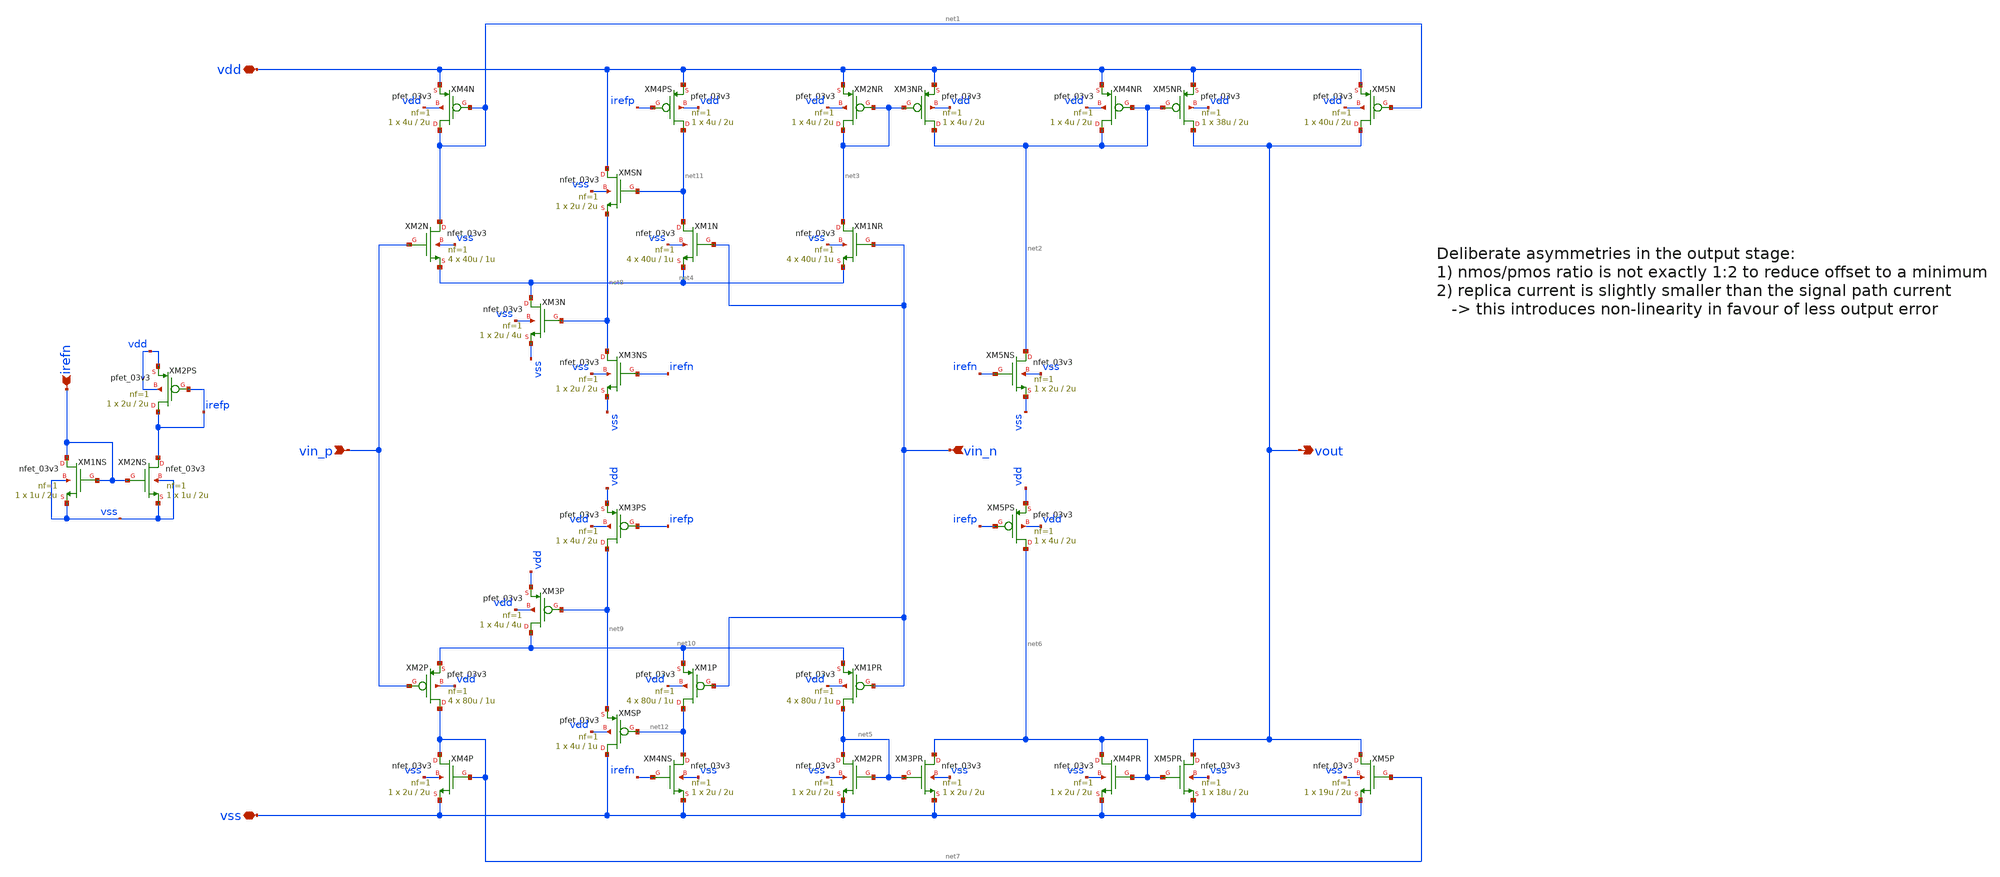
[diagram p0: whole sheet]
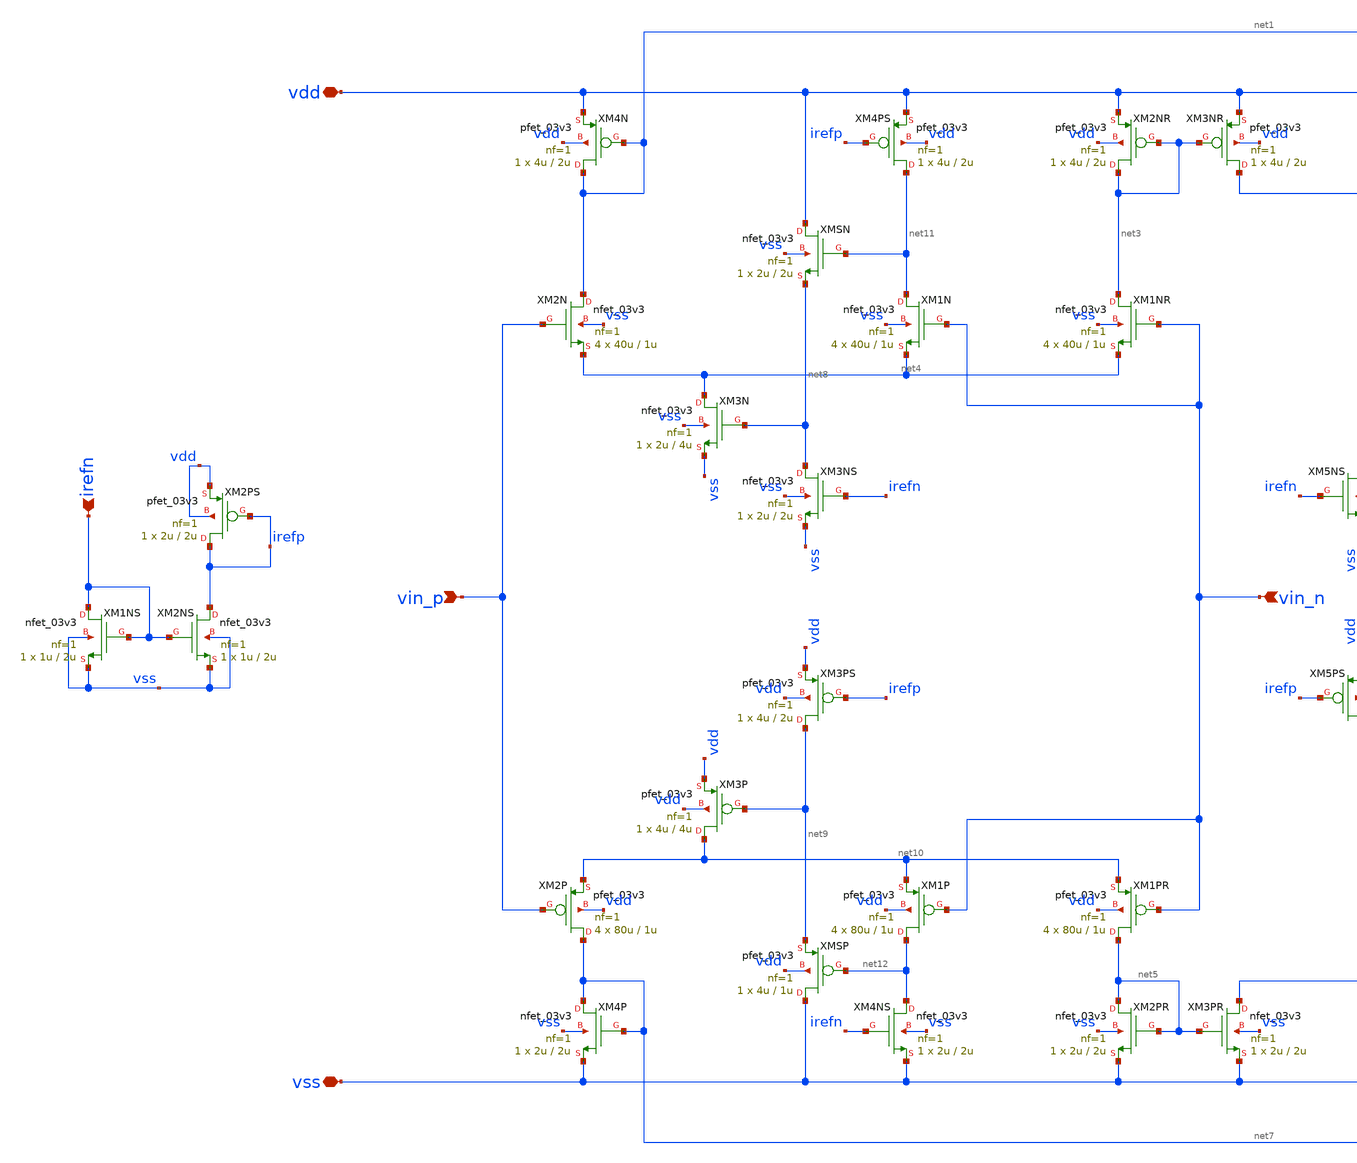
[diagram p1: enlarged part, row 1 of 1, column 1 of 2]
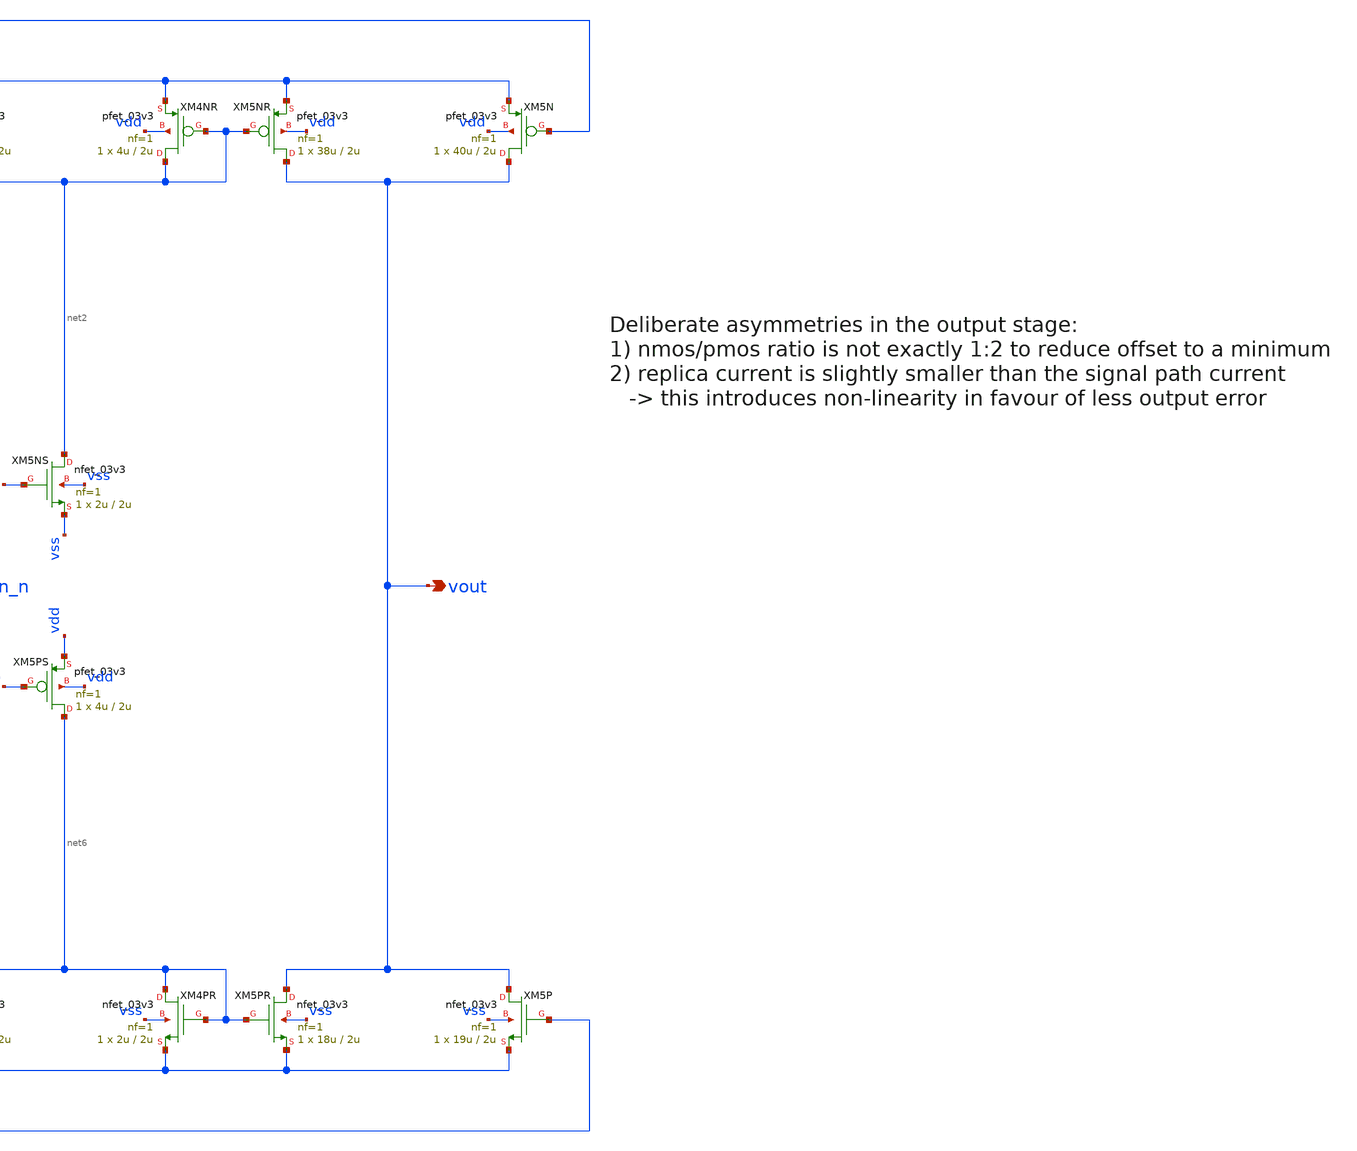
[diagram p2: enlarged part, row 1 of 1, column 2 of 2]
** sch_path: General/ADC/analogbuffer/analogbuffer-openloop.sch
**.subckt analogbuffer-openloop vdd vss vin_p vout irefn vin_n
*.iopin vdd
*.iopin vss
*.ipin vin_p
*.opin vout
*.ipin irefn
*.ipin vin_n
XM2P net7 vin_p net10 vdd pfet_03v3 L=1u W=80u nf=1 ad='int((nf+1)/2) * W/nf * 0.18u' as='int((nf+2)/2) * W/nf * 0.18u'
+ pd='2*int((nf+1)/2) * (W/nf + 0.18u)' ps='2*int((nf+2)/2) * (W/nf + 0.18u)' nrd='0.18u / W' nrs='0.18u / W'
+ sa=0 sb=0 sd=0 m=4
XM2N net1 vin_p net4 vss nfet_03v3 L=1u W=40u nf=1 ad='int((nf+1)/2) * W/nf * 0.18u' as='int((nf+2)/2) * W/nf * 0.18u'
+ pd='2*int((nf+1)/2) * (W/nf + 0.18u)' ps='2*int((nf+2)/2) * (W/nf + 0.18u)' nrd='0.18u / W' nrs='0.18u / W'
+ sa=0 sb=0 sd=0 m=4
XM3N net4 net8 vss vss nfet_03v3 L=4u W=2u nf=1 ad='int((nf+1)/2) * W/nf * 0.18u' as='int((nf+2)/2) * W/nf * 0.18u'
+ pd='2*int((nf+1)/2) * (W/nf + 0.18u)' ps='2*int((nf+2)/2) * (W/nf + 0.18u)' nrd='0.18u / W' nrs='0.18u / W'
+ sa=0 sb=0 sd=0 m=1
XM1NR net3 vin_n net4 vss nfet_03v3 L=1u W=40u nf=1 ad='int((nf+1)/2) * W/nf * 0.18u' as='int((nf+2)/2) * W/nf * 0.18u'
+ pd='2*int((nf+1)/2) * (W/nf + 0.18u)' ps='2*int((nf+2)/2) * (W/nf + 0.18u)' nrd='0.18u / W' nrs='0.18u / W'
+ sa=0 sb=0 sd=0 m=4
XM2NR net3 net3 vdd vdd pfet_03v3 L=2u W=4u nf=1 ad='int((nf+1)/2) * W/nf * 0.18u' as='int((nf+2)/2) * W/nf * 0.18u'
+ pd='2*int((nf+1)/2) * (W/nf + 0.18u)' ps='2*int((nf+2)/2) * (W/nf + 0.18u)' nrd='0.18u / W' nrs='0.18u / W'
+ sa=0 sb=0 sd=0 m=1
XM3NR net2 net3 vdd vdd pfet_03v3 L=2u W=4u nf=1 ad='int((nf+1)/2) * W/nf * 0.18u' as='int((nf+2)/2) * W/nf * 0.18u'
+ pd='2*int((nf+1)/2) * (W/nf + 0.18u)' ps='2*int((nf+2)/2) * (W/nf + 0.18u)' nrd='0.18u / W' nrs='0.18u / W'
+ sa=0 sb=0 sd=0 m=1
XM4NR net2 net2 vdd vdd pfet_03v3 L=2u W=4u nf=1 ad='int((nf+1)/2) * W/nf * 0.18u' as='int((nf+2)/2) * W/nf * 0.18u'
+ pd='2*int((nf+1)/2) * (W/nf + 0.18u)' ps='2*int((nf+2)/2) * (W/nf + 0.18u)' nrd='0.18u / W' nrs='0.18u / W'
+ sa=0 sb=0 sd=0 m=1
XM5NR vout net2 vdd vdd pfet_03v3 L=2u W=38u nf=1 ad='int((nf+1)/2) * W/nf * 0.18u' as='int((nf+2)/2) * W/nf * 0.18u'
+ pd='2*int((nf+1)/2) * (W/nf + 0.18u)' ps='2*int((nf+2)/2) * (W/nf + 0.18u)' nrd='0.18u / W' nrs='0.18u / W'
+ sa=0 sb=0 sd=0 m=1
XM5N vout net1 vdd vdd pfet_03v3 L=2u W=40u nf=1 ad='int((nf+1)/2) * W/nf * 0.18u' as='int((nf+2)/2) * W/nf * 0.18u'
+ pd='2*int((nf+1)/2) * (W/nf + 0.18u)' ps='2*int((nf+2)/2) * (W/nf + 0.18u)' nrd='0.18u / W' nrs='0.18u / W'
+ sa=0 sb=0 sd=0 m=1
XM4N net1 net1 vdd vdd pfet_03v3 L=2u W=4u nf=1 ad='int((nf+1)/2) * W/nf * 0.18u' as='int((nf+2)/2) * W/nf * 0.18u'
+ pd='2*int((nf+1)/2) * (W/nf + 0.18u)' ps='2*int((nf+2)/2) * (W/nf + 0.18u)' nrd='0.18u / W' nrs='0.18u / W'
+ sa=0 sb=0 sd=0 m=1
XM5NS net2 irefn vss vss nfet_03v3 L=2u W=2u nf=1 ad='int((nf+1)/2) * W/nf * 0.18u' as='int((nf+2)/2) * W/nf * 0.18u'
+ pd='2*int((nf+1)/2) * (W/nf + 0.18u)' ps='2*int((nf+2)/2) * (W/nf + 0.18u)' nrd='0.18u / W' nrs='0.18u / W'
+ sa=0 sb=0 sd=0 m=1
XM1PR net5 vin_n net10 vdd pfet_03v3 L=1u W=80u nf=1 ad='int((nf+1)/2) * W/nf * 0.18u' as='int((nf+2)/2) * W/nf * 0.18u'
+ pd='2*int((nf+1)/2) * (W/nf + 0.18u)' ps='2*int((nf+2)/2) * (W/nf + 0.18u)' nrd='0.18u / W' nrs='0.18u / W'
+ sa=0 sb=0 sd=0 m=4
XM3P net10 net9 vdd vdd pfet_03v3 L=4u W=4u nf=1 ad='int((nf+1)/2) * W/nf * 0.18u' as='int((nf+2)/2) * W/nf * 0.18u'
+ pd='2*int((nf+1)/2) * (W/nf + 0.18u)' ps='2*int((nf+2)/2) * (W/nf + 0.18u)' nrd='0.18u / W' nrs='0.18u / W'
+ sa=0 sb=0 sd=0 m=1
XM2PR net5 net5 vss vss nfet_03v3 L=2u W=2u nf=1 ad='int((nf+1)/2) * W/nf * 0.18u' as='int((nf+2)/2) * W/nf * 0.18u'
+ pd='2*int((nf+1)/2) * (W/nf + 0.18u)' ps='2*int((nf+2)/2) * (W/nf + 0.18u)' nrd='0.18u / W' nrs='0.18u / W'
+ sa=0 sb=0 sd=0 m=1
XM3PR net6 net5 vss vss nfet_03v3 L=2u W=2u nf=1 ad='int((nf+1)/2) * W/nf * 0.18u' as='int((nf+2)/2) * W/nf * 0.18u'
+ pd='2*int((nf+1)/2) * (W/nf + 0.18u)' ps='2*int((nf+2)/2) * (W/nf + 0.18u)' nrd='0.18u / W' nrs='0.18u / W'
+ sa=0 sb=0 sd=0 m=1
XM4PR net6 net6 vss vss nfet_03v3 L=2u W=2u nf=1 ad='int((nf+1)/2) * W/nf * 0.18u' as='int((nf+2)/2) * W/nf * 0.18u'
+ pd='2*int((nf+1)/2) * (W/nf + 0.18u)' ps='2*int((nf+2)/2) * (W/nf + 0.18u)' nrd='0.18u / W' nrs='0.18u / W'
+ sa=0 sb=0 sd=0 m=1
XM5PR vout net6 vss vss nfet_03v3 L=2u W=18u nf=1 ad='int((nf+1)/2) * W/nf * 0.18u' as='int((nf+2)/2) * W/nf * 0.18u'
+ pd='2*int((nf+1)/2) * (W/nf + 0.18u)' ps='2*int((nf+2)/2) * (W/nf + 0.18u)' nrd='0.18u / W' nrs='0.18u / W'
+ sa=0 sb=0 sd=0 m=1
XM5PS net6 irefp vdd vdd pfet_03v3 L=2u W=4u nf=1 ad='int((nf+1)/2) * W/nf * 0.18u' as='int((nf+2)/2) * W/nf * 0.18u'
+ pd='2*int((nf+1)/2) * (W/nf + 0.18u)' ps='2*int((nf+2)/2) * (W/nf + 0.18u)' nrd='0.18u / W' nrs='0.18u / W'
+ sa=0 sb=0 sd=0 m=1
XM5P vout net7 vss vss nfet_03v3 L=2u W=19u nf=1 ad='int((nf+1)/2) * W/nf * 0.18u' as='int((nf+2)/2) * W/nf * 0.18u'
+ pd='2*int((nf+1)/2) * (W/nf + 0.18u)' ps='2*int((nf+2)/2) * (W/nf + 0.18u)' nrd='0.18u / W' nrs='0.18u / W'
+ sa=0 sb=0 sd=0 m=1
XM4P net7 net7 vss vss nfet_03v3 L=2u W=2u nf=1 ad='int((nf+1)/2) * W/nf * 0.18u' as='int((nf+2)/2) * W/nf * 0.18u'
+ pd='2*int((nf+1)/2) * (W/nf + 0.18u)' ps='2*int((nf+2)/2) * (W/nf + 0.18u)' nrd='0.18u / W' nrs='0.18u / W'
+ sa=0 sb=0 sd=0 m=1
XM2NS irefp irefn vss vss nfet_03v3 L=2u W=1u nf=1 ad='int((nf+1)/2) * W/nf * 0.18u' as='int((nf+2)/2) * W/nf * 0.18u'
+ pd='2*int((nf+1)/2) * (W/nf + 0.18u)' ps='2*int((nf+2)/2) * (W/nf + 0.18u)' nrd='0.18u / W' nrs='0.18u / W'
+ sa=0 sb=0 sd=0 m=1
XM1NS irefn irefn vss vss nfet_03v3 L=2u W=1u nf=1 ad='int((nf+1)/2) * W/nf * 0.18u' as='int((nf+2)/2) * W/nf * 0.18u'
+ pd='2*int((nf+1)/2) * (W/nf + 0.18u)' ps='2*int((nf+2)/2) * (W/nf + 0.18u)' nrd='0.18u / W' nrs='0.18u / W'
+ sa=0 sb=0 sd=0 m=1
XM2PS irefp irefp vdd vdd pfet_03v3 L=2u W=2u nf=1 ad='int((nf+1)/2) * W/nf * 0.18u' as='int((nf+2)/2) * W/nf * 0.18u'
+ pd='2*int((nf+1)/2) * (W/nf + 0.18u)' ps='2*int((nf+2)/2) * (W/nf + 0.18u)' nrd='0.18u / W' nrs='0.18u / W'
+ sa=0 sb=0 sd=0 m=1
XMSN vdd net11 net8 vss nfet_03v3 L=2u W=2u nf=1 ad='int((nf+1)/2) * W/nf * 0.18u' as='int((nf+2)/2) * W/nf * 0.18u'
+ pd='2*int((nf+1)/2) * (W/nf + 0.18u)' ps='2*int((nf+2)/2) * (W/nf + 0.18u)' nrd='0.18u / W' nrs='0.18u / W'
+ sa=0 sb=0 sd=0 m=1
XM3NS net8 irefn vss vss nfet_03v3 L=2u W=2u nf=1 ad='int((nf+1)/2) * W/nf * 0.18u' as='int((nf+2)/2) * W/nf * 0.18u'
+ pd='2*int((nf+1)/2) * (W/nf + 0.18u)' ps='2*int((nf+2)/2) * (W/nf + 0.18u)' nrd='0.18u / W' nrs='0.18u / W'
+ sa=0 sb=0 sd=0 m=1
XM1N net11 vin_n net4 vss nfet_03v3 L=1u W=40u nf=1 ad='int((nf+1)/2) * W/nf * 0.18u' as='int((nf+2)/2) * W/nf * 0.18u'
+ pd='2*int((nf+1)/2) * (W/nf + 0.18u)' ps='2*int((nf+2)/2) * (W/nf + 0.18u)' nrd='0.18u / W' nrs='0.18u / W'
+ sa=0 sb=0 sd=0 m=4
XM4PS net11 irefp vdd vdd pfet_03v3 L=2u W=4u nf=1 ad='int((nf+1)/2) * W/nf * 0.18u' as='int((nf+2)/2) * W/nf * 0.18u'
+ pd='2*int((nf+1)/2) * (W/nf + 0.18u)' ps='2*int((nf+2)/2) * (W/nf + 0.18u)' nrd='0.18u / W' nrs='0.18u / W'
+ sa=0 sb=0 sd=0 m=1
XM3PS net9 irefp vdd vdd pfet_03v3 L=2u W=4u nf=1 ad='int((nf+1)/2) * W/nf * 0.18u' as='int((nf+2)/2) * W/nf * 0.18u'
+ pd='2*int((nf+1)/2) * (W/nf + 0.18u)' ps='2*int((nf+2)/2) * (W/nf + 0.18u)' nrd='0.18u / W' nrs='0.18u / W'
+ sa=0 sb=0 sd=0 m=1
XM1P net12 vin_n net10 vdd pfet_03v3 L=1u W=80u nf=1 ad='int((nf+1)/2) * W/nf * 0.18u' as='int((nf+2)/2) * W/nf * 0.18u'
+ pd='2*int((nf+1)/2) * (W/nf + 0.18u)' ps='2*int((nf+2)/2) * (W/nf + 0.18u)' nrd='0.18u / W' nrs='0.18u / W'
+ sa=0 sb=0 sd=0 m=4
XM4NS net12 irefn vss vss nfet_03v3 L=2u W=2u nf=1 ad='int((nf+1)/2) * W/nf * 0.18u' as='int((nf+2)/2) * W/nf * 0.18u'
+ pd='2*int((nf+1)/2) * (W/nf + 0.18u)' ps='2*int((nf+2)/2) * (W/nf + 0.18u)' nrd='0.18u / W' nrs='0.18u / W'
+ sa=0 sb=0 sd=0 m=1
XMSP vss net12 net9 vdd pfet_03v3 L=1u W=4u nf=1 ad='int((nf+1)/2) * W/nf * 0.18u' as='int((nf+2)/2) * W/nf * 0.18u'
+ pd='2*int((nf+1)/2) * (W/nf + 0.18u)' ps='2*int((nf+2)/2) * (W/nf + 0.18u)' nrd='0.18u / W' nrs='0.18u / W'
+ sa=0 sb=0 sd=0 m=1
**.ends
.end
